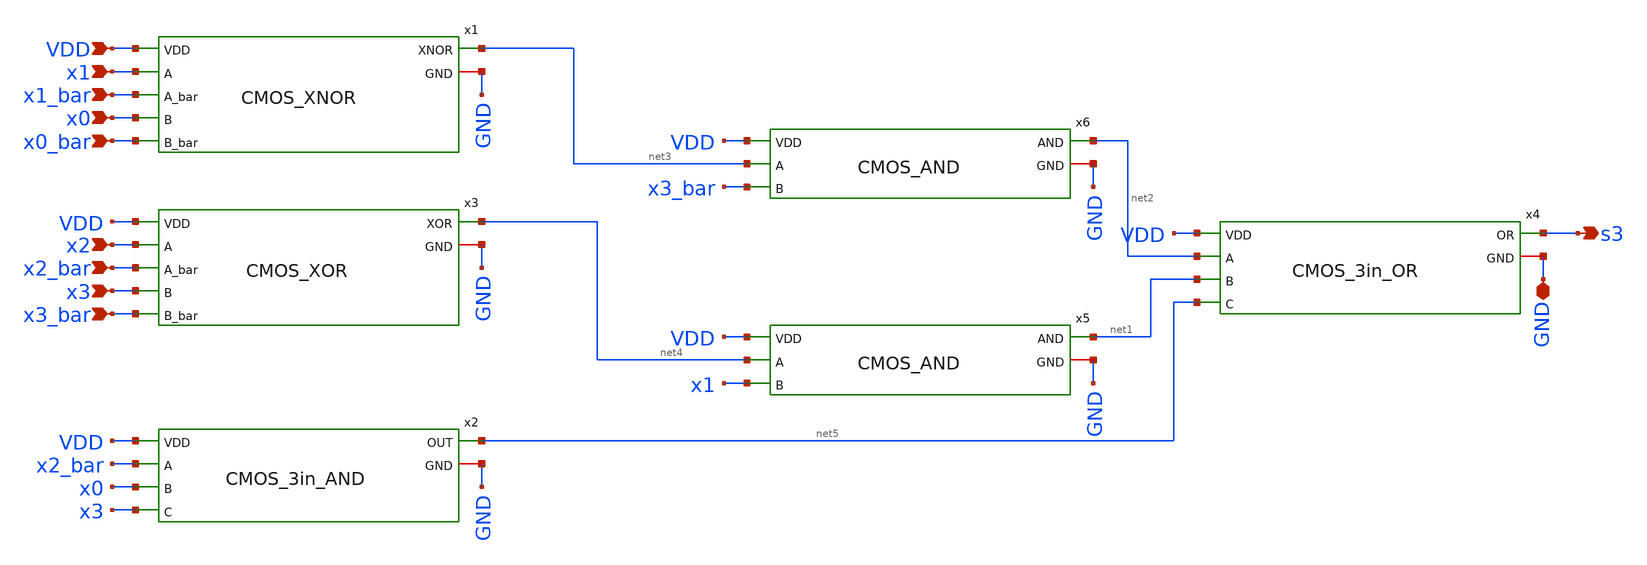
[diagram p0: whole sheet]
** sch_path: skywater_stuff/CMOS_s3_flat.sch
**.subckt CMOS_s3_flat GND x0 x0_bar x1 x1_bar x2 x2_bar x3 x3_bar s3 VDD
*.iopin GND
*.ipin x0
*.ipin x0_bar
*.ipin x1
*.ipin x1_bar
*.ipin x2
*.ipin x2_bar
*.ipin x3
*.ipin x3_bar
*.opin s3
*.ipin VDD
x5 net4 x1 net1 GND VDD CMOS_AND
x6 net3 x3_bar net2 GND VDD CMOS_AND
x2 x2_bar x0 x3 net5 GND VDD CMOS_3in_AND
x4 net2 net1 net5 s3 GND VDD CMOS_3in_OR
x1 x1 x1_bar x0 x0_bar net3 GND VDD CMOS_XNOR
x3 x2 x2_bar x3 x3_bar net4 GND VDD CMOS_XOR
**.ends
.end
